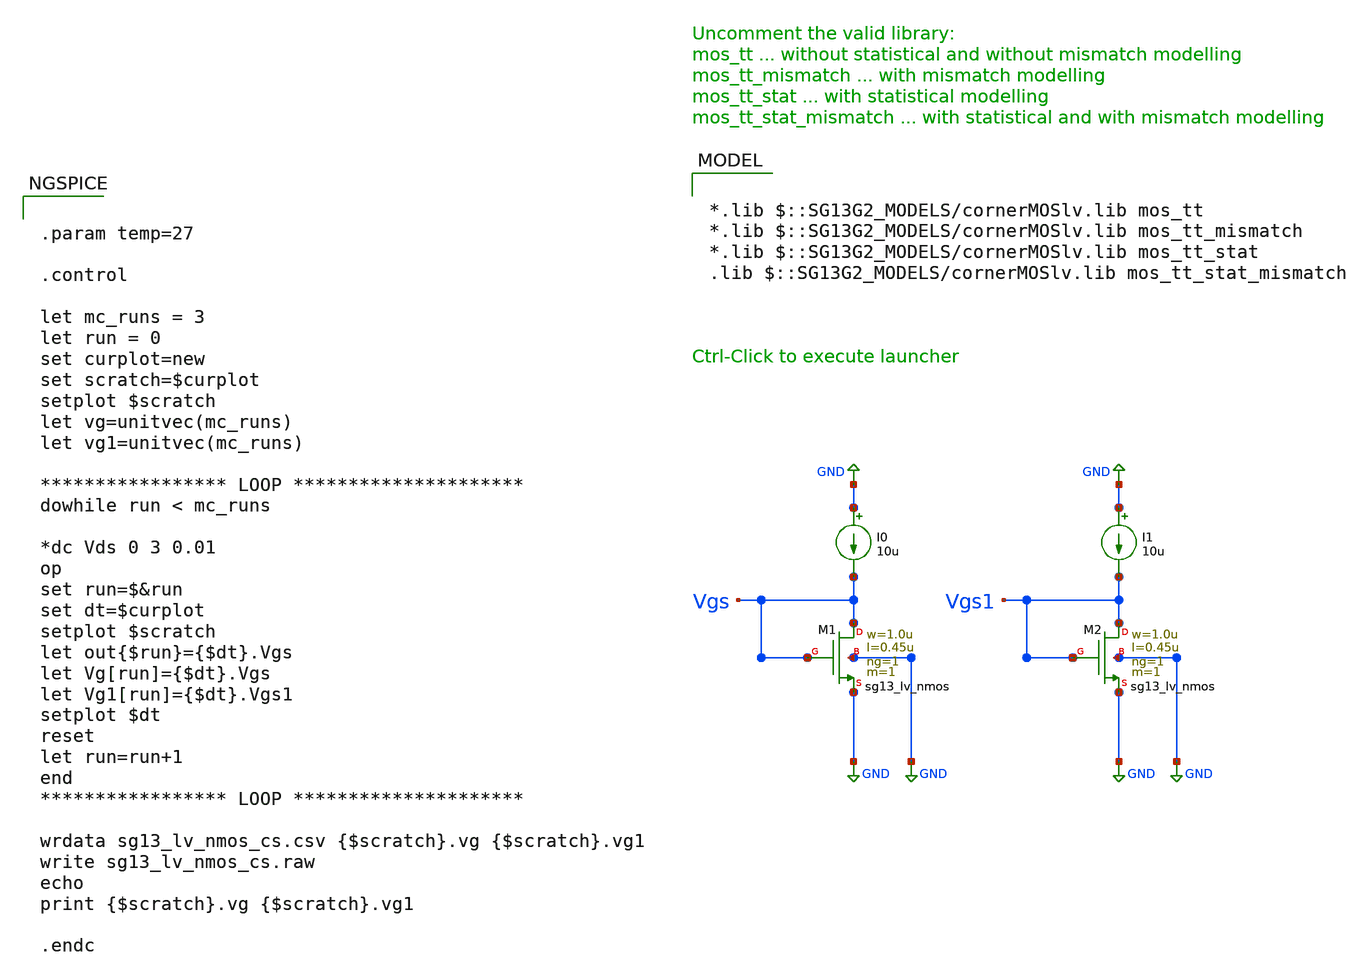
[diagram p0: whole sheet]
** sch_path: ihp-sg13g2/libs.tech/xschem/sg13g2_tests/mc_lv_nmos_cs_loop.sch
* Copyright 2023 IHP PDK Authors
**.subckt mc_lv_nmos_cs_loop
I0 GND Vgs 10u
XM1 Vgs Vgs GND GND sg13_lv_nmos w=1.0u l=0.45u ng=1 m=1 mm_ok=1
I1 GND Vgs1 10u
XM2 Vgs1 Vgs1 GND GND sg13_lv_nmos w=1.0u l=0.45u ng=1 m=1 mm_ok=1
I0 GND Vgs 10u
XM1 Vgs Vgs GND GND sg13_lv_nmos w=1.0u l=0.45u ng=1 m=1 mm_ok=1
I1 GND Vgs1 10u
XM2 Vgs1 Vgs1 GND GND sg13_lv_nmos w=1.0u l=0.45u ng=1 m=1 mm_ok=1
**** begin user architecture code


.param temp=27

.control

let mc_runs = 3
let run = 0
set curplot=new
set scratch=$curplot
setplot $scratch
let vg=unitvec(mc_runs)
let vg1=unitvec(mc_runs)

***************** LOOP *********************
dowhile run < mc_runs

*dc Vds 0 3 0.01
op
set run=$&run
set dt=$curplot
setplot $scratch
let out{$run}={$dt}.Vgs
let Vg[run]={$dt}.Vgs
let Vg1[run]={$dt}.Vgs1
setplot $dt
reset
let run=run+1
end
***************** LOOP *********************

wrdata sg13_lv_nmos_cs.csv {$scratch}.vg {$scratch}.vg1
write sg13_lv_nmos_cs.raw
echo
print {$scratch}.vg {$scratch}.vg1

.endc



*.lib $::SG13G2_MODELS/cornerMOSlv.lib mos_tt
*.lib $::SG13G2_MODELS/cornerMOSlv.lib mos_tt_mismatch
*.lib $::SG13G2_MODELS/cornerMOSlv.lib mos_tt_stat
.lib $::SG13G2_MODELS/cornerMOSlv.lib mos_tt_stat_mismatch



.param temp=27

.control

let mc_runs = 3
let run = 0
set curplot=new
set scratch=$curplot
setplot $scratch
let vg=unitvec(mc_runs)
let vg1=unitvec(mc_runs)

***************** LOOP *********************
dowhile run < mc_runs

*dc Vds 0 3 0.01
op
set run=$&run
set dt=$curplot
setplot $scratch
let out{$run}={$dt}.Vgs
let Vg[run]={$dt}.Vgs
let Vg1[run]={$dt}.Vgs1
setplot $dt
reset
let run=run+1
end
***************** LOOP *********************

wrdata sg13_lv_nmos_cs.csv {$scratch}.vg {$scratch}.vg1
write sg13_lv_nmos_cs.raw
echo
print {$scratch}.vg {$scratch}.vg1

.endc



*.lib $::SG13G2_MODELS/cornerMOSlv.lib mos_tt
*.lib $::SG13G2_MODELS/cornerMOSlv.lib mos_tt_mismatch
*.lib $::SG13G2_MODELS/cornerMOSlv.lib mos_tt_stat
.lib $::SG13G2_MODELS/cornerMOSlv.lib mos_tt_stat_mismatch

**** end user architecture code
**.ends
.GLOBAL GND
.end
